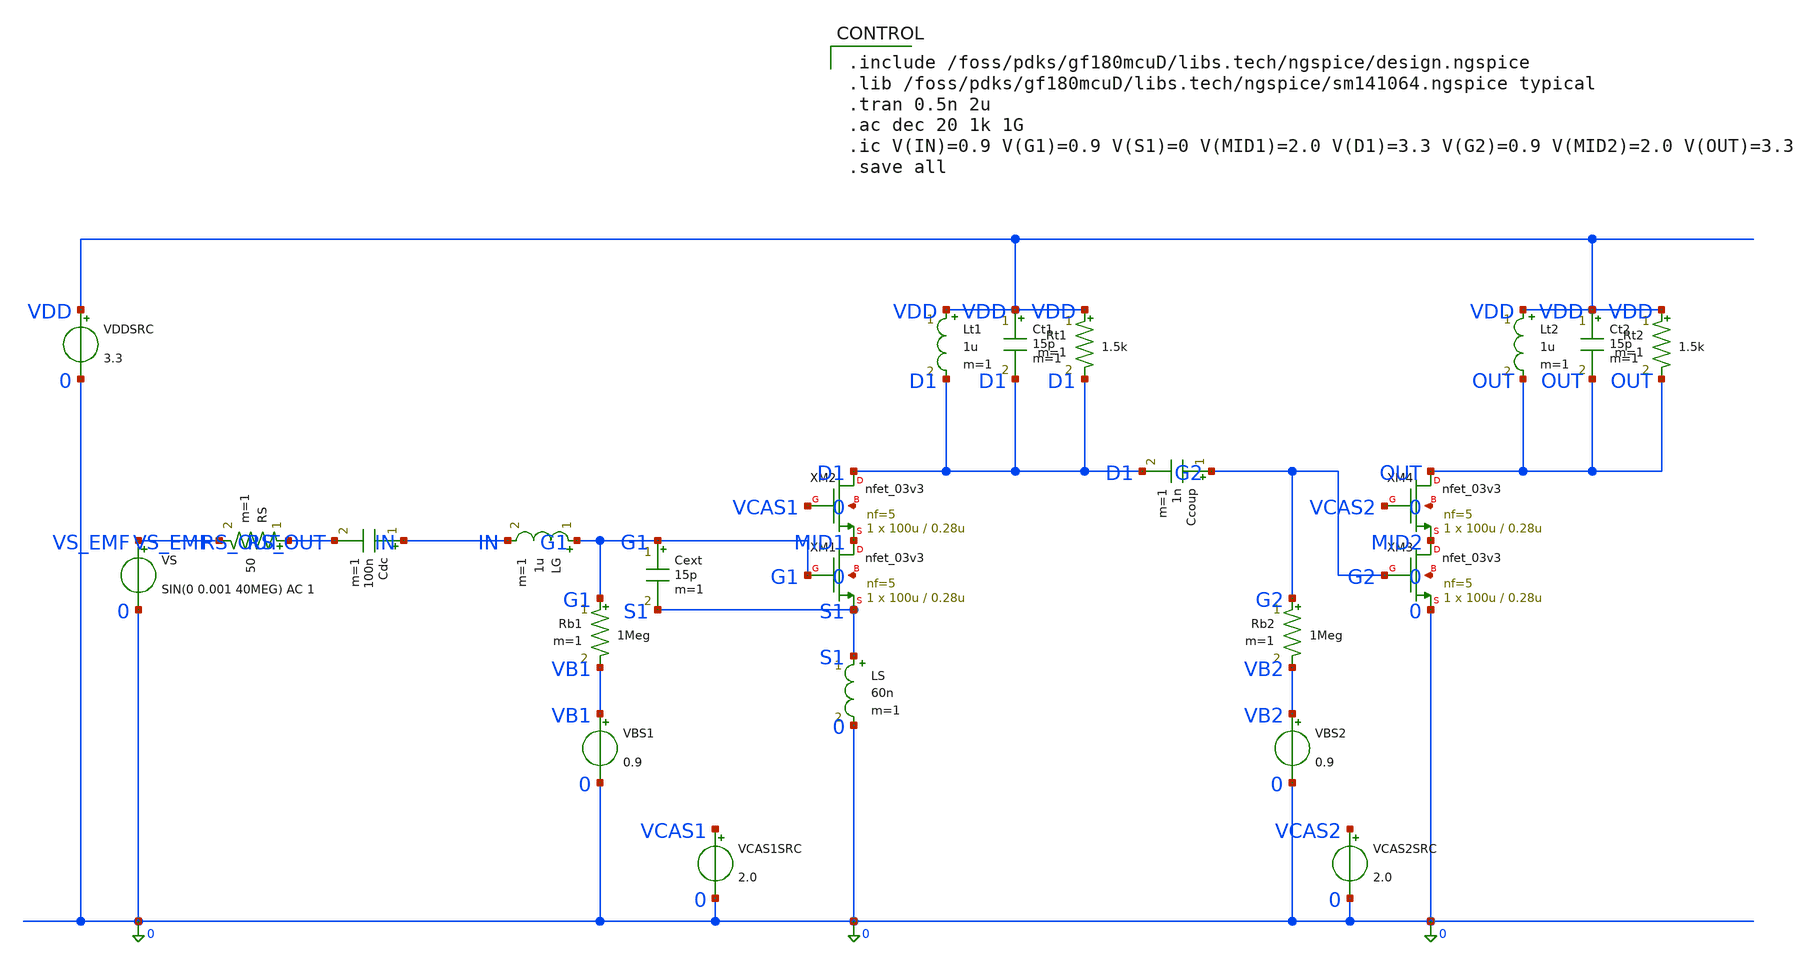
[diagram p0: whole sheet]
** sch_path: modules/PandaChip/designs/lna-match/lna_match_v4.sch
**.subckt lna_match_v4
VS VS_EMF 0 SIN(0 0.001 40MEG) AC 1
RS RS_OUT VS_EMF 50 m=1
Cdc IN RS_OUT 100n m=1
LG G1 IN 1u m=1
Cext G1 S1 15p m=1
XM1 MID1 G1 S1 0 nfet_03v3 L=0.28u W=100u nf=5 ad='int((nf+1)/2) * W/nf * 0.18u' as='int((nf+2)/2) * W/nf * 0.18u'
+ pd='2*int((nf+1)/2) * (W/nf + 0.18u)' ps='2*int((nf+2)/2) * (W/nf + 0.18u)' nrd='0.18u / W' nrs='0.18u / W'
+ sa=0 sb=0 sd=0 m=1
LS S1 0 60n m=1
XM2 D1 VCAS1 MID1 0 nfet_03v3 L=0.28u W=100u nf=5 ad='int((nf+1)/2) * W/nf * 0.18u' as='int((nf+2)/2) * W/nf * 0.18u'
+ pd='2*int((nf+1)/2) * (W/nf + 0.18u)' ps='2*int((nf+2)/2) * (W/nf + 0.18u)' nrd='0.18u / W' nrs='0.18u / W'
+ sa=0 sb=0 sd=0 m=1
Lt1 VDD D1 1u m=1
Ct1 VDD D1 15p m=1
Rt1 VDD D1 1.5k m=1
Ccoup G2 D1 1n m=1
Rb1 G1 VB1 1Meg m=1
VBS1 VB1 0 0.9
Rb2 G2 VB2 1Meg m=1
VBS2 VB2 0 0.9
XM3 MID2 G2 0 0 nfet_03v3 L=0.28u W=100u nf=5 ad='int((nf+1)/2) * W/nf * 0.18u' as='int((nf+2)/2) * W/nf * 0.18u'
+ pd='2*int((nf+1)/2) * (W/nf + 0.18u)' ps='2*int((nf+2)/2) * (W/nf + 0.18u)' nrd='0.18u / W' nrs='0.18u / W'
+ sa=0 sb=0 sd=0 m=1
XM4 OUT VCAS2 MID2 0 nfet_03v3 L=0.28u W=100u nf=5 ad='int((nf+1)/2) * W/nf * 0.18u' as='int((nf+2)/2) * W/nf * 0.18u'
+ pd='2*int((nf+1)/2) * (W/nf + 0.18u)' ps='2*int((nf+2)/2) * (W/nf + 0.18u)' nrd='0.18u / W' nrs='0.18u / W'
+ sa=0 sb=0 sd=0 m=1
Lt2 VDD OUT 1u m=1
Ct2 VDD OUT 15p m=1
Rt2 VDD OUT 1.5k m=1
VDDSRC VDD 0 3.3
VCAS1SRC VCAS1 0 2.0
VCAS2SRC VCAS2 0 2.0
**** begin user architecture code

.include /foss/pdks/gf180mcuD/libs.tech/ngspice/design.ngspice
.lib /foss/pdks/gf180mcuD/libs.tech/ngspice/sm141064.ngspice typical
.tran 0.5n 2u
.ac dec 20 1k 1G
.ic V(IN)=0.9 V(G1)=0.9 V(S1)=0 V(MID1)=2.0 V(D1)=3.3 V(G2)=0.9 V(MID2)=2.0 V(OUT)=3.3
.save all

**** end user architecture code
**.ends
.end
